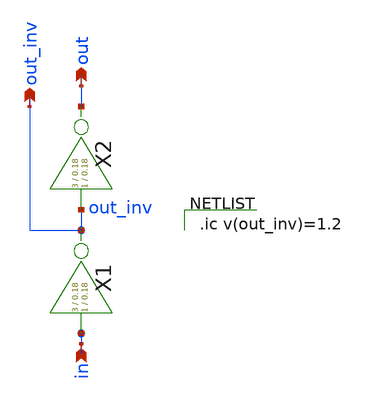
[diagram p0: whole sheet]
** sch_path: xschem/decoder/bottom_peripheral_cell.sch
**.subckt bottom_peripheral_cell out out_inv in
*.opin out
*.opin out_inv
*.ipin in
X2 out_inv out inv Wpmos=3 Lpmos=0.18 Wnmos=1 Lnmos=0.18
X1 in out_inv inv Wpmos=3 Lpmos=0.18 Wnmos=1 Lnmos=0.18
**** begin user architecture code

.ic v(out_inv)=1.2

**** end user architecture code
**.ends

* expanding   symbol:  inv/inv.sym # of pins=2
** sym_path: xschem/inv/inv.sym
** sch_path: xschem/inv/inv.sch
.subckt inv in out  Wpmos=3 Lpmos=0.18 Wnmos=1 Lnmos=0.18
*.ipin in
*.iopin out
XM1 out in GND GND sky130_fd_pr__nfet_01v8 L=Lnmos W=Wnmos nf=1 ad='int((nf+1)/2) * W/nf * 0.29' as='int((nf+2)/2) * W/nf * 0.29'
+ pd='2*int((nf+1)/2) * (W/nf + 0.29)' ps='2*int((nf+2)/2) * (W/nf + 0.29)' nrd='0.29 / W' nrs='0.29 / W'
+ sa=0 sb=0 sd=0 mult=1 m=1
XM2 out in VDD VDD sky130_fd_pr__pfet_01v8 L=Lpmos W=Wpmos nf=1 ad='int((nf+1)/2) * W/nf * 0.29' as='int((nf+2)/2) * W/nf * 0.29'
+ pd='2*int((nf+1)/2) * (W/nf + 0.29)' ps='2*int((nf+2)/2) * (W/nf + 0.29)' nrd='0.29 / W' nrs='0.29 / W'
+ sa=0 sb=0 sd=0 mult=1 m=1
.ends

.GLOBAL VDD
.GLOBAL GND
.end
